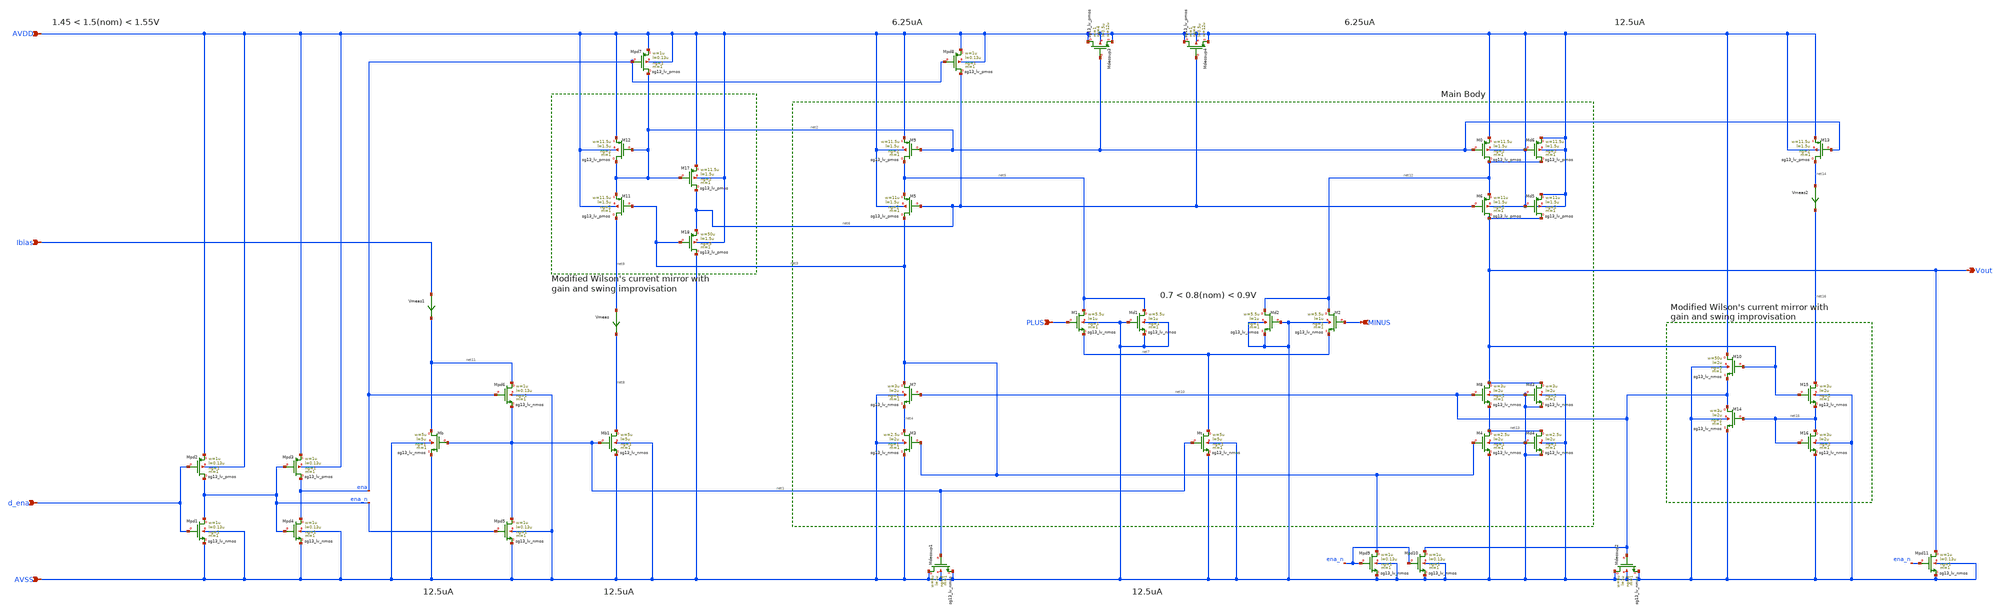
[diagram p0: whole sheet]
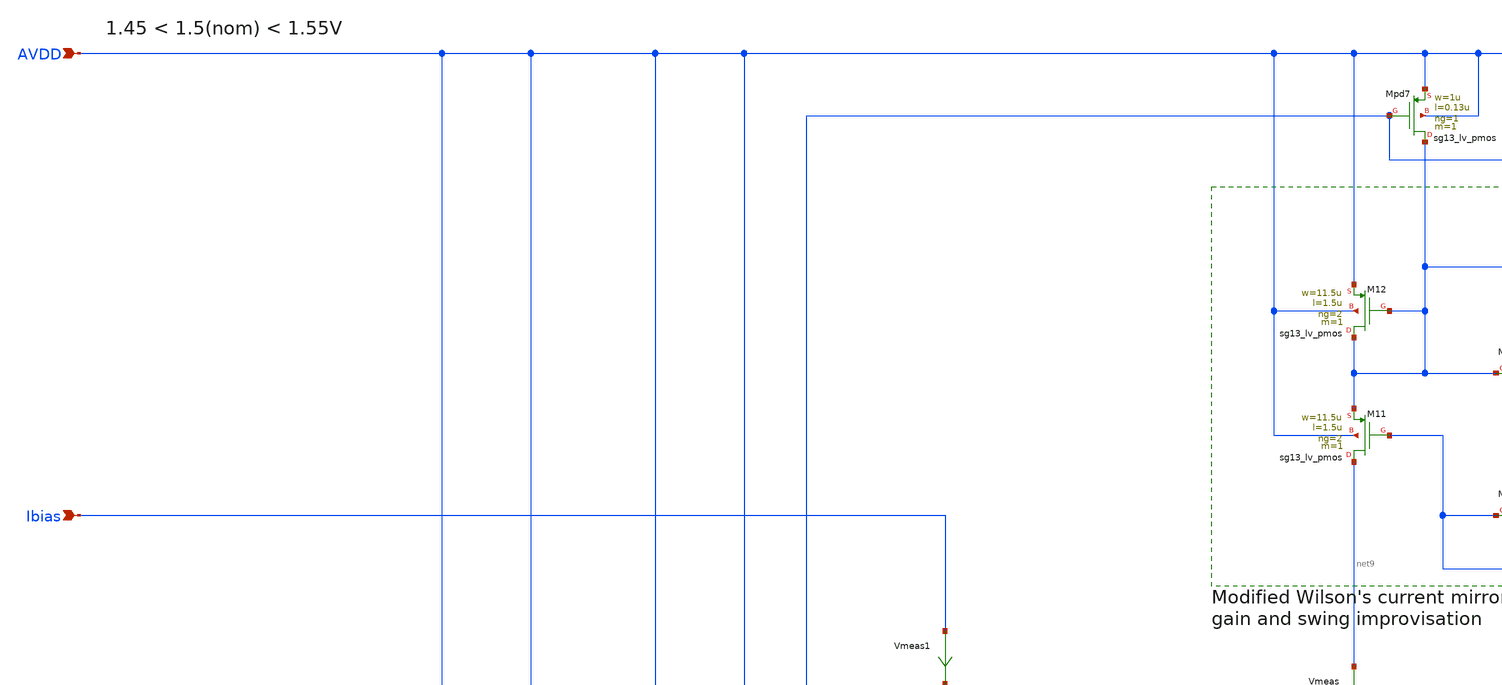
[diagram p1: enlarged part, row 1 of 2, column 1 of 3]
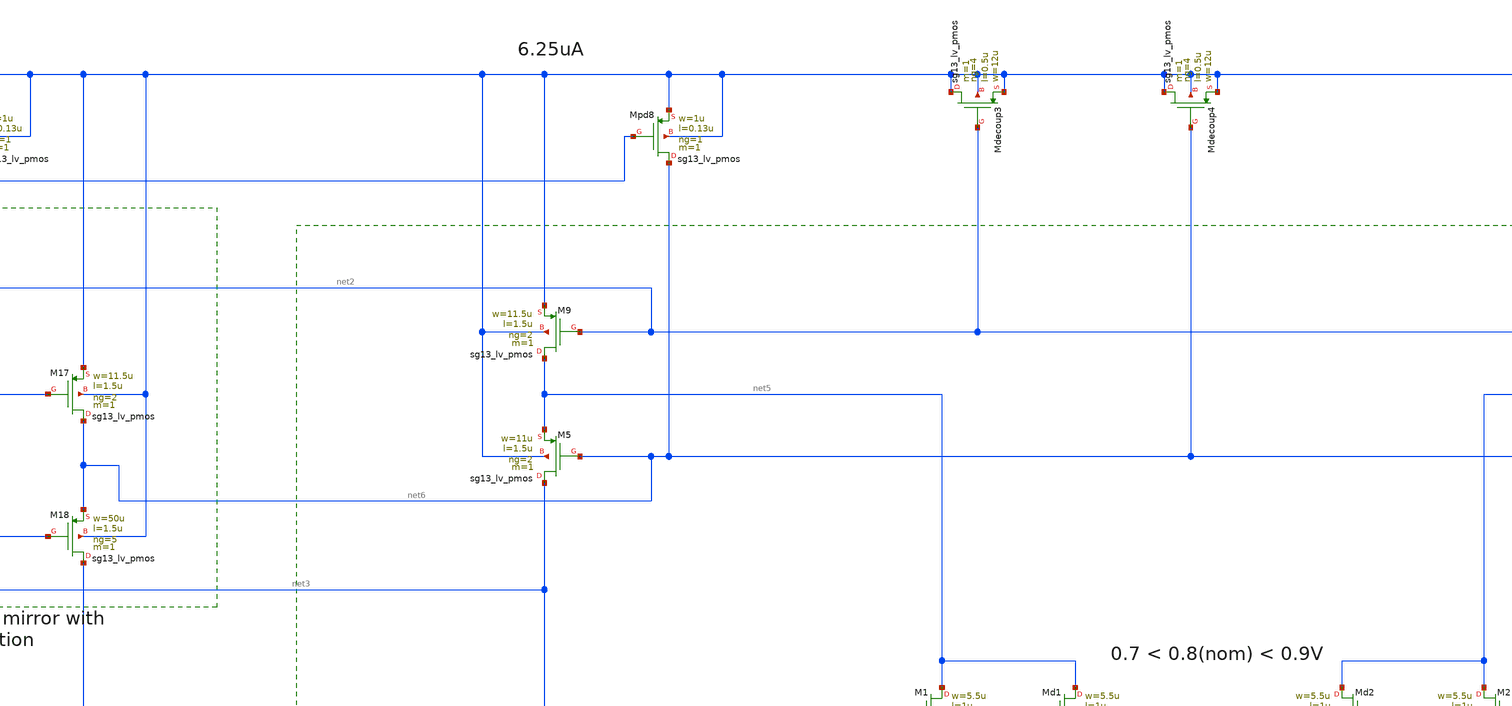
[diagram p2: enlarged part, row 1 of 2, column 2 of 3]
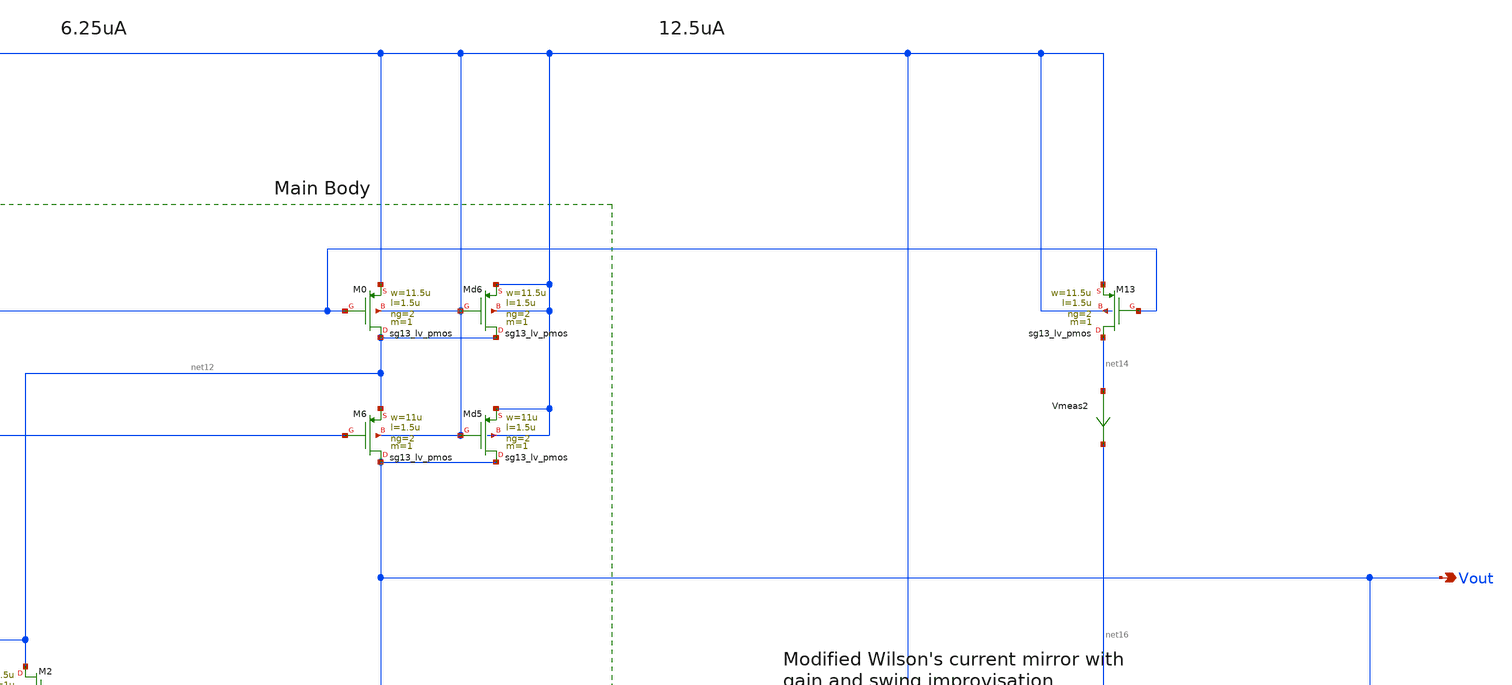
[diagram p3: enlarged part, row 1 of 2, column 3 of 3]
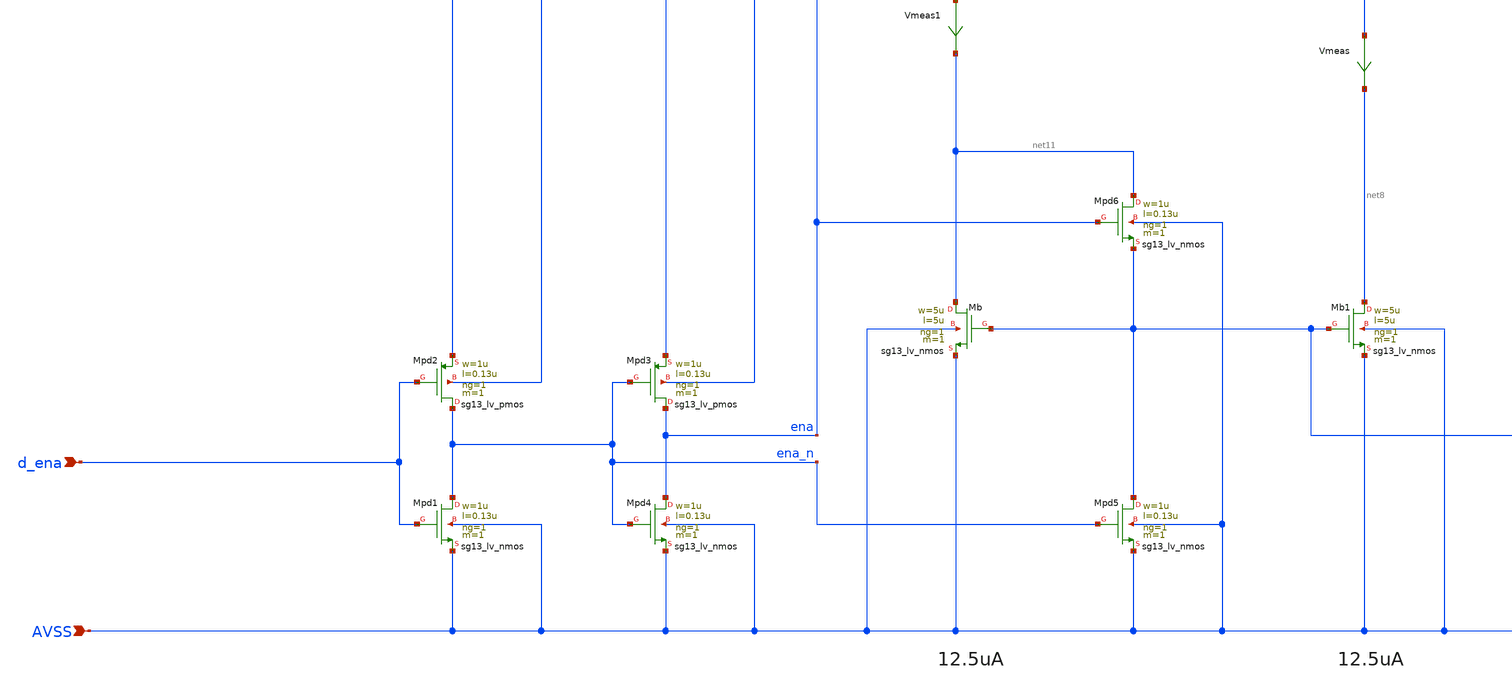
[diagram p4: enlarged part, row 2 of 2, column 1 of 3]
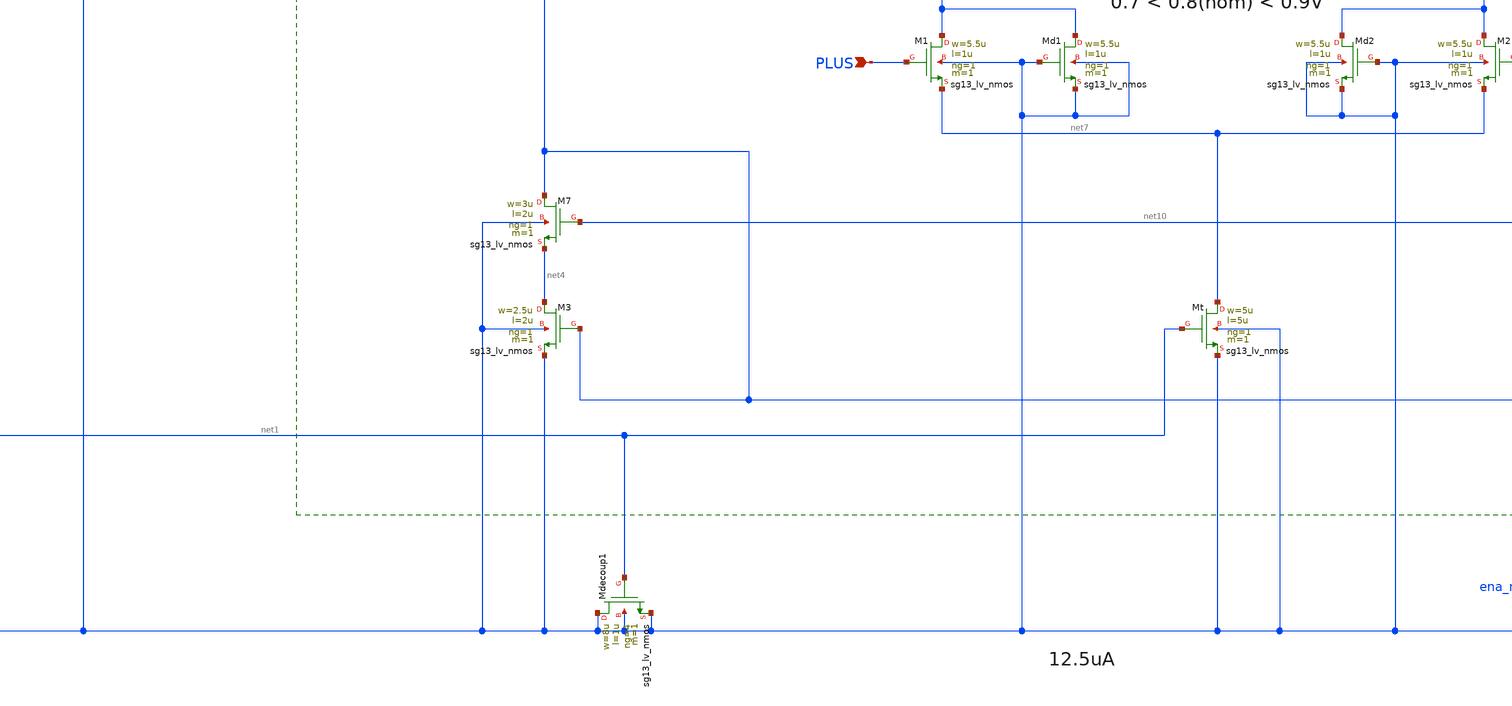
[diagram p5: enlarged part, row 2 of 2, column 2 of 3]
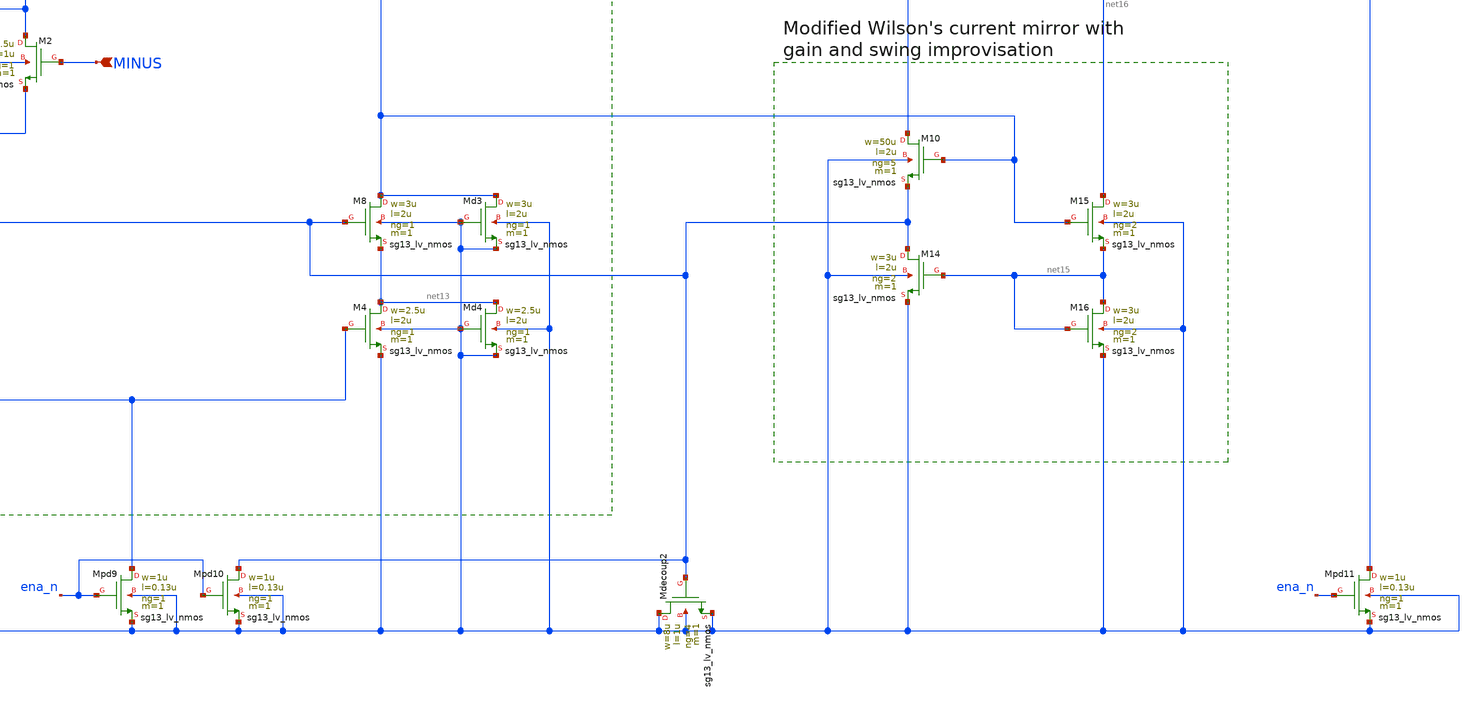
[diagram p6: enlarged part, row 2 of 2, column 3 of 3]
** sch_path: Designs/otas/1_schematics/foldedcascode_nmos_withdummies.sch
* (c) 2025 Thesis_HP, Apache-2.0 license
**.subckt foldedcascode_nmos_withdummies AVSS Ibias AVDD PLUS MINUS Vout d_ena
*.ipin AVSS
*.ipin Ibias
*.ipin AVDD
*.ipin PLUS
*.ipin MINUS
*.opin Vout
*.ipin d_ena
XMb net11 net1 AVSS AVSS sg13_lv_nmos w=5u l=5u ng=1 m=1 mm_ok=1
XMpd5 net1 ena_n AVSS AVSS sg13_lv_nmos w=1u l=0.13u ng=1 m=1 mm_ok=1
XMpd6 net11 ena net1 AVSS sg13_lv_nmos w=1u l=0.13u ng=1 m=1 mm_ok=1
XMb1 net8 net1 AVSS AVSS sg13_lv_nmos w=5u l=5u ng=1 m=1 mm_ok=1
Vmeas net9 net8 0
.save i(vmeas)
XM11 net9 net3 net2 AVDD sg13_lv_pmos w=11.5u l=1.5u ng=2 m=1 mm_ok=1
XM12 net2 net2 AVDD AVDD sg13_lv_pmos w=11.5u l=1.5u ng=2 m=1 mm_ok=1
XM18 AVSS net3 net6 AVDD sg13_lv_pmos w=50u l=1.5u ng=5 m=1 mm_ok=1
XM17 net6 net2 AVDD AVDD sg13_lv_pmos w=11.5u l=1.5u ng=2 m=1 mm_ok=1
XM9 net5 net2 AVDD AVDD sg13_lv_pmos w=11.5u l=1.5u ng=2 m=1 mm_ok=1
XM5 net3 net6 net5 AVDD sg13_lv_pmos w=11u l=1.5u ng=2 m=1 mm_ok=1
XM7 net3 net10 net4 AVSS sg13_lv_nmos w=3u l=2u ng=1 m=1 mm_ok=1
XM3 net4 net3 AVSS AVSS sg13_lv_nmos w=2.5u l=2u ng=1 m=1 mm_ok=1
XMpd7 net2 ena AVDD AVDD sg13_lv_pmos w=1u l=0.13u ng=1 m=1 mm_ok=1
XMpd8 net6 ena AVDD AVDD sg13_lv_pmos w=1u l=0.13u ng=1 m=1 mm_ok=1
XMt net7 net1 AVSS AVSS sg13_lv_nmos w=5u l=5u ng=1 m=1 mm_ok=1
XM1 net5 PLUS net7 AVSS sg13_lv_nmos w=5.5u l=1u ng=1 m=1 mm_ok=1
XM2 net12 MINUS net7 AVSS sg13_lv_nmos w=5.5u l=1u ng=1 m=1 mm_ok=1
XMdecoup3 AVDD net2 AVDD AVDD sg13_lv_pmos w=12u l=0.5u ng=4 m=1 mm_ok=1
XMdecoup4 AVDD net6 AVDD AVDD sg13_lv_pmos w=12u l=0.5u ng=4 m=1 mm_ok=1
XMdecoup1 AVSS net1 AVSS AVSS sg13_lv_nmos w=8u l=1u ng=4 m=1 mm_ok=1
XMpd2 ena_n d_ena AVDD AVDD sg13_lv_pmos w=1u l=0.13u ng=1 m=1 mm_ok=1
Vmeas1 Ibias net11 0
.save i(vmeas1)
XMpd3 ena ena_n AVDD AVDD sg13_lv_pmos w=1u l=0.13u ng=1 m=1 mm_ok=1
XMpd1 ena_n d_ena AVSS AVSS sg13_lv_nmos w=1u l=0.13u ng=1 m=1 mm_ok=1
XMpd4 ena ena_n AVSS AVSS sg13_lv_nmos w=1u l=0.13u ng=1 m=1 mm_ok=1
XMd2 net12 AVSS AVSS AVSS sg13_lv_nmos w=5.5u l=1u ng=1 m=1 mm_ok=1
XM6 Vout net6 net12 AVDD sg13_lv_pmos w=11u l=1.5u ng=2 m=1 mm_ok=1
XM0 net12 net2 AVDD AVDD sg13_lv_pmos w=11.5u l=1.5u ng=2 m=1 mm_ok=1
XM8 Vout net10 net13 AVSS sg13_lv_nmos w=3u l=2u ng=1 m=1 mm_ok=1
XM4 net13 net3 AVSS AVSS sg13_lv_nmos w=2.5u l=2u ng=1 m=1 mm_ok=1
XMd4 net13 AVSS AVSS AVSS sg13_lv_nmos w=2.5u l=2u ng=1 m=1 mm_ok=1
XMd3 Vout AVSS AVSS AVSS sg13_lv_nmos w=3u l=2u ng=1 m=1 mm_ok=1
XMd6 net12 AVDD AVDD AVDD sg13_lv_pmos w=11.5u l=1.5u ng=2 m=1 mm_ok=1
XMd5 Vout AVDD AVDD AVDD sg13_lv_pmos w=11u l=1.5u ng=2 m=1 mm_ok=1
XM13 net14 net2 AVDD AVDD sg13_lv_pmos w=11.5u l=1.5u ng=2 m=1 mm_ok=1
Vmeas2 net14 net16 0
.save i(vmeas2)
XM15 net16 Vout net15 AVSS sg13_lv_nmos w=3u l=2u ng=2 m=1 mm_ok=1
XM16 net15 net15 AVSS AVSS sg13_lv_nmos w=3u l=2u ng=2 m=1 mm_ok=1
XM14 net10 net15 AVSS AVSS sg13_lv_nmos w=3u l=2u ng=2 m=1 mm_ok=1
XM10 AVDD Vout net10 AVSS sg13_lv_nmos w=50u l=2u ng=5 m=1 mm_ok=1
XMpd11 Vout ena_n AVSS AVSS sg13_lv_nmos w=1u l=0.13u ng=1 m=1 mm_ok=1
XMdecoup2 AVSS net10 AVSS AVSS sg13_lv_nmos w=8u l=1u ng=4 m=1 mm_ok=1
XMpd10 net10 ena_n AVSS AVSS sg13_lv_nmos w=1u l=0.13u ng=1 m=1 mm_ok=1
XMpd9 net3 ena_n AVSS AVSS sg13_lv_nmos w=1u l=0.13u ng=1 m=1 mm_ok=1
XMd1 net5 AVSS AVSS AVSS sg13_lv_nmos w=5.5u l=1u ng=1 m=1 mm_ok=1
**.ends
.end
